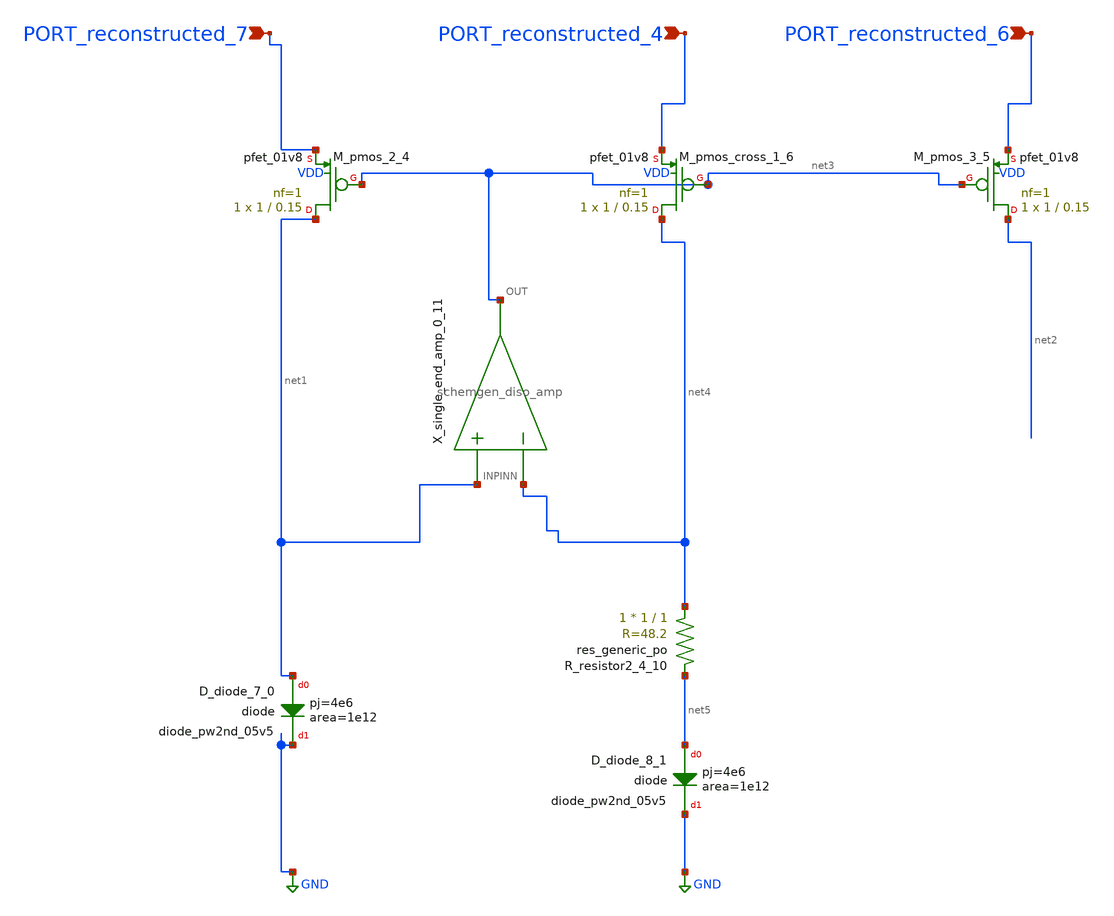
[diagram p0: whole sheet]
** sch_path: schematics/Image2Net/115.sch
**.subckt 115 PORT_reconstructed_6 PORT_reconstructed_4 PORT_reconstructed_7
*.ipin PORT_reconstructed_6
*.ipin PORT_reconstructed_4
*.ipin PORT_reconstructed_7
XD_diode_7_0 net1 GND sky130_fd_pr__diode_pw2nd_05v5 area=1e12 pj=4e6
XD_diode_8_1 net5 GND sky130_fd_pr__diode_pw2nd_05v5 area=1e12 pj=4e6
XM_pmos_2_4 net1 net3 PORT_reconstructed_7 VDD sky130_fd_pr__pfet_01v8 L=0.15 W=1 nf=1 ad='int((1 + 1)/2) * 1 / 1 * 0.29'
+ as='int((1 + 2)/2) * 1 / 1 * 0.29' pd='2*int((1 + 1)/2) * (1 / 1 + 0.29)' ps='2*int((1 + 2)/2) * (1 / 1 + 0.29)'
+ nrd='0.29 / 1 ' nrs='0.29 / 1 ' sa=0 sb=0 sd=0 mult=1 m=1
XM_pmos_3_5 net2 net3 PORT_reconstructed_6 VDD sky130_fd_pr__pfet_01v8 L=0.15 W=1 nf=1 ad='int((1 + 1)/2) * 1 / 1 * 0.29'
+ as='int((1 + 2)/2) * 1 / 1 * 0.29' pd='2*int((1 + 1)/2) * (1 / 1 + 0.29)' ps='2*int((1 + 2)/2) * (1 / 1 + 0.29)'
+ nrd='0.29 / 1 ' nrs='0.29 / 1 ' sa=0 sb=0 sd=0 mult=1 m=1
XM_pmos_cross_1_6 net4 net3 PORT_reconstructed_4 VDD sky130_fd_pr__pfet_01v8 L=0.15 W=1 nf=1 ad='int((1 + 1)/2) * 1 / 1 * 0.29'
+ as='int((1 + 2)/2) * 1 / 1 * 0.29' pd='2*int((1 + 1)/2) * (1 / 1 + 0.29)' ps='2*int((1 + 2)/2) * (1 / 1 + 0.29)'
+ nrd='0.29 / 1 ' nrs='0.29 / 1 ' sa=0 sb=0 sd=0 mult=1 m=1
XR_resistor2_4_10 net4 net5 sky130_fd_pr__res_generic_po W=1 L=1 m=1
X_single_end_amp_0_11 net1 net4 net3 schemgen_diso_amp
**.ends

* expanding   symbol:  schemgen_diso_amp.sym # of pins=3
** sym_path: symbols/schemgen_diso_amp.sym
.subckt schemgen_diso_amp INP INN OUT
* SchemGen ideal op-amp: Vout = 1e5 * (V(INP) - V(INN))
E1 OUT 0 INP INN 1e5
.ends schemgen_diso_amp
.GLOBAL GND
.end
